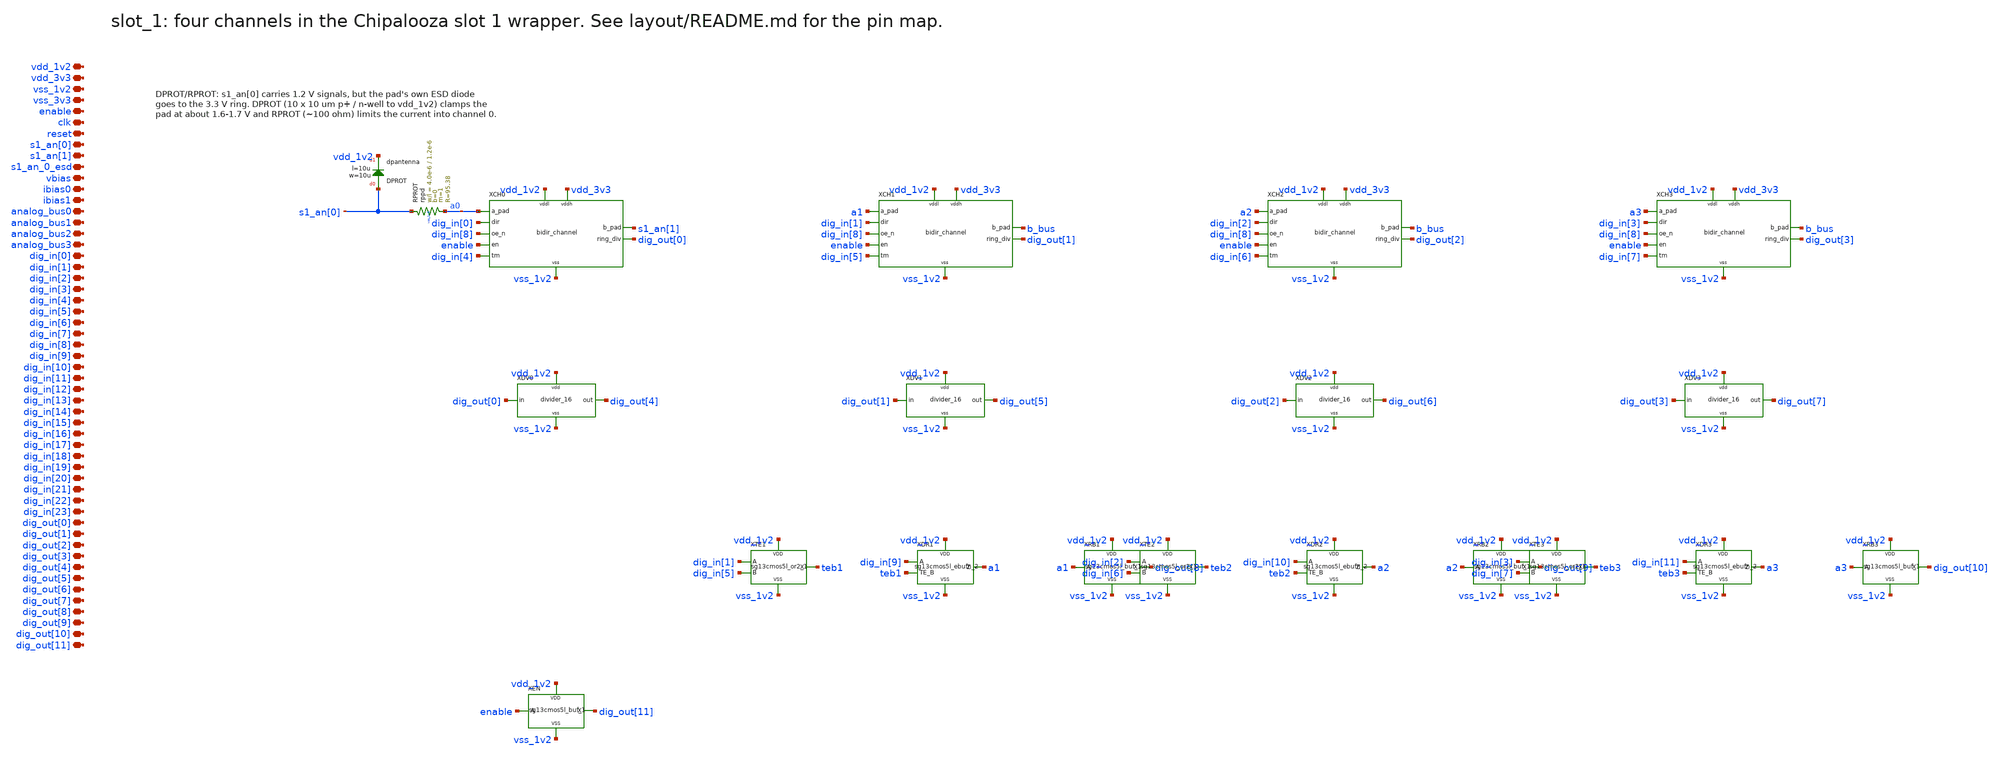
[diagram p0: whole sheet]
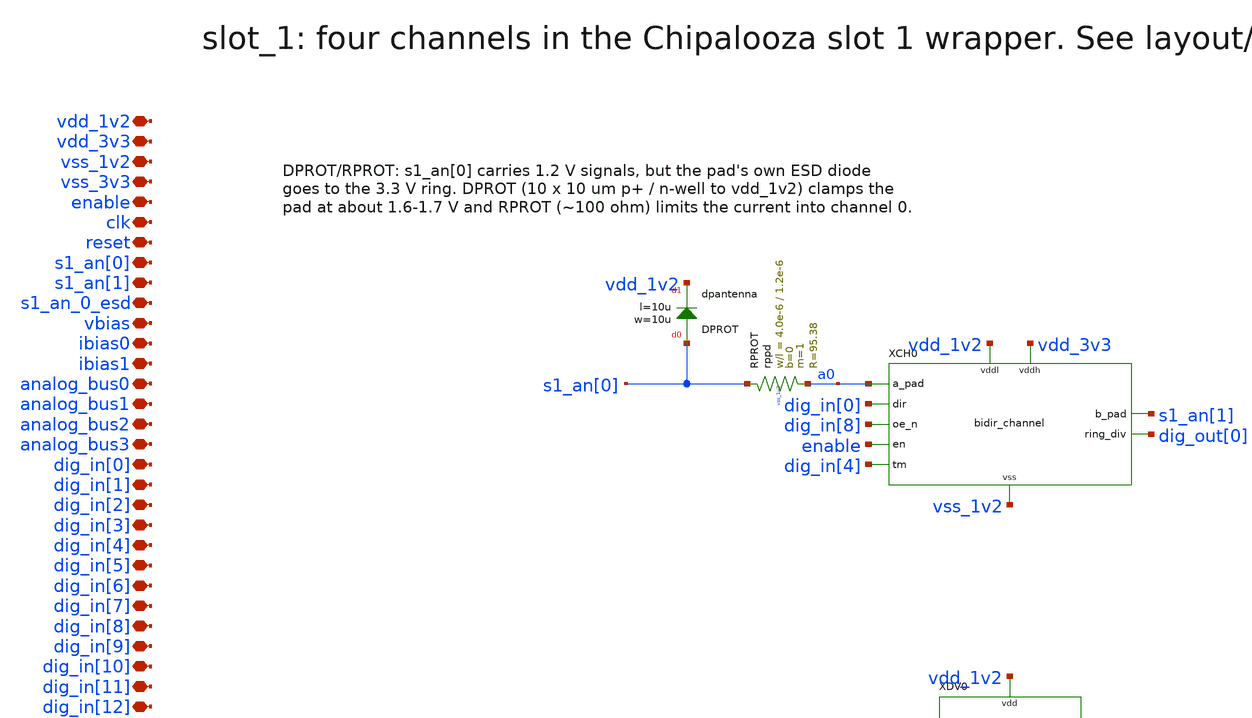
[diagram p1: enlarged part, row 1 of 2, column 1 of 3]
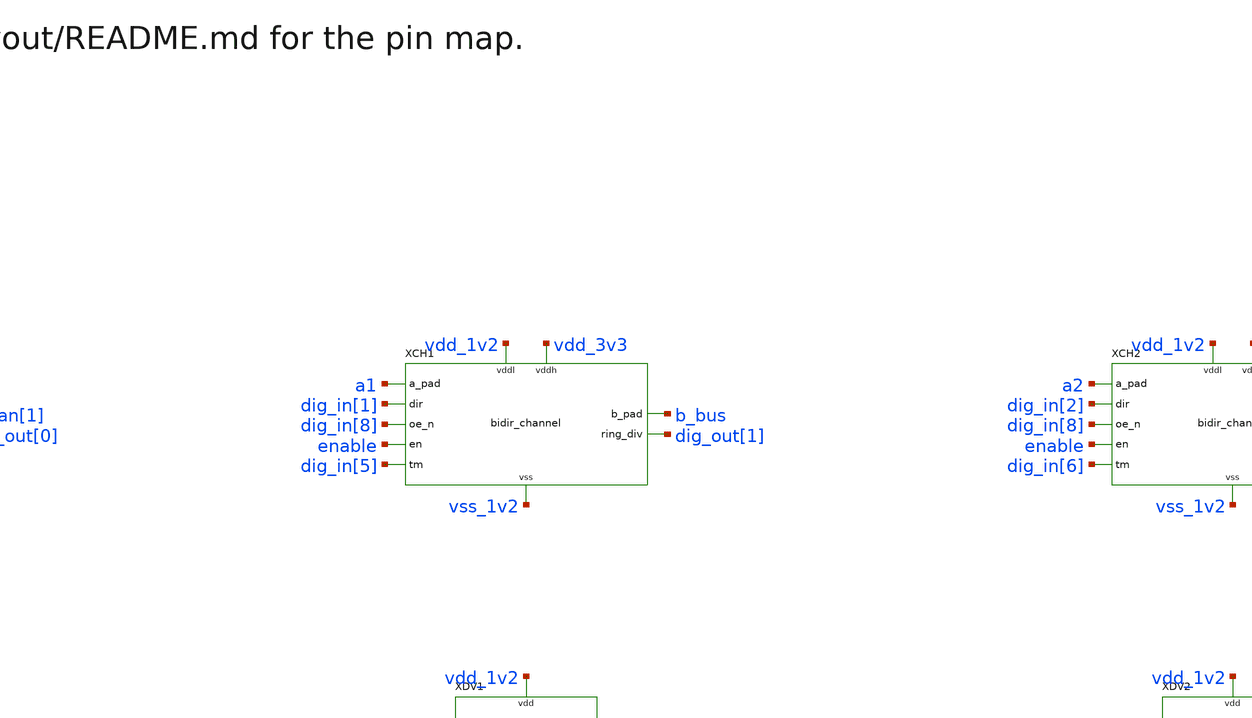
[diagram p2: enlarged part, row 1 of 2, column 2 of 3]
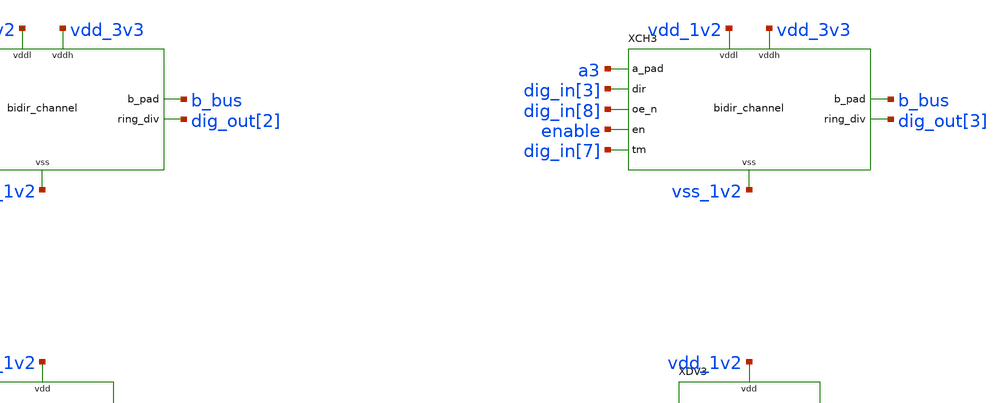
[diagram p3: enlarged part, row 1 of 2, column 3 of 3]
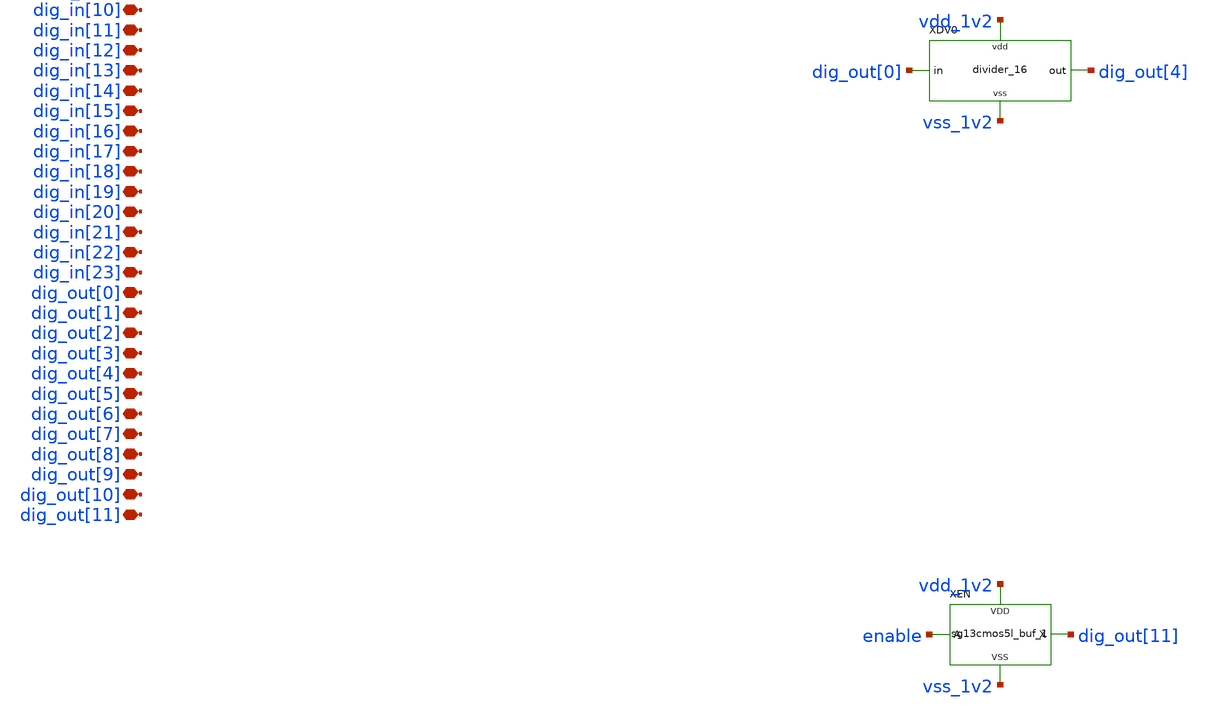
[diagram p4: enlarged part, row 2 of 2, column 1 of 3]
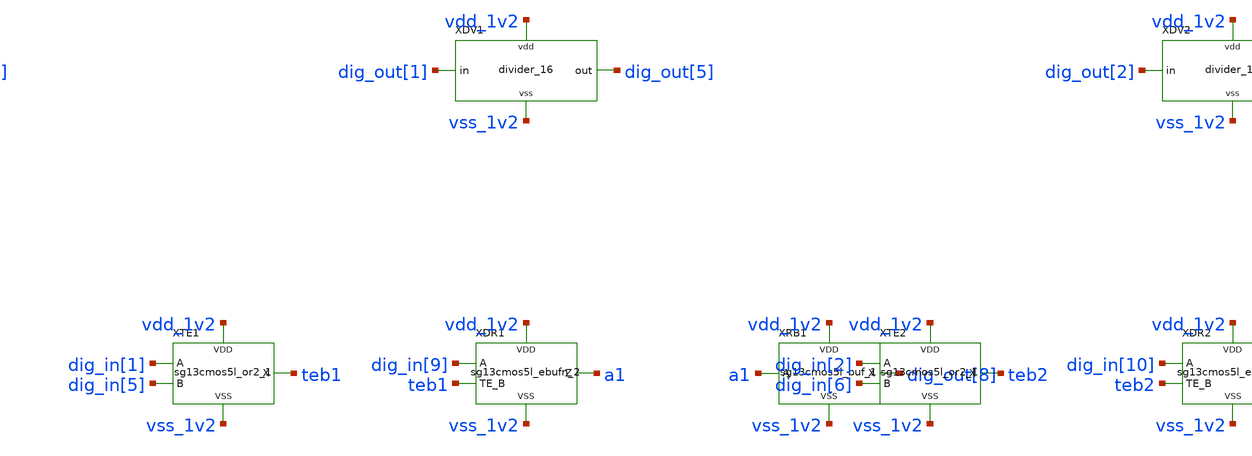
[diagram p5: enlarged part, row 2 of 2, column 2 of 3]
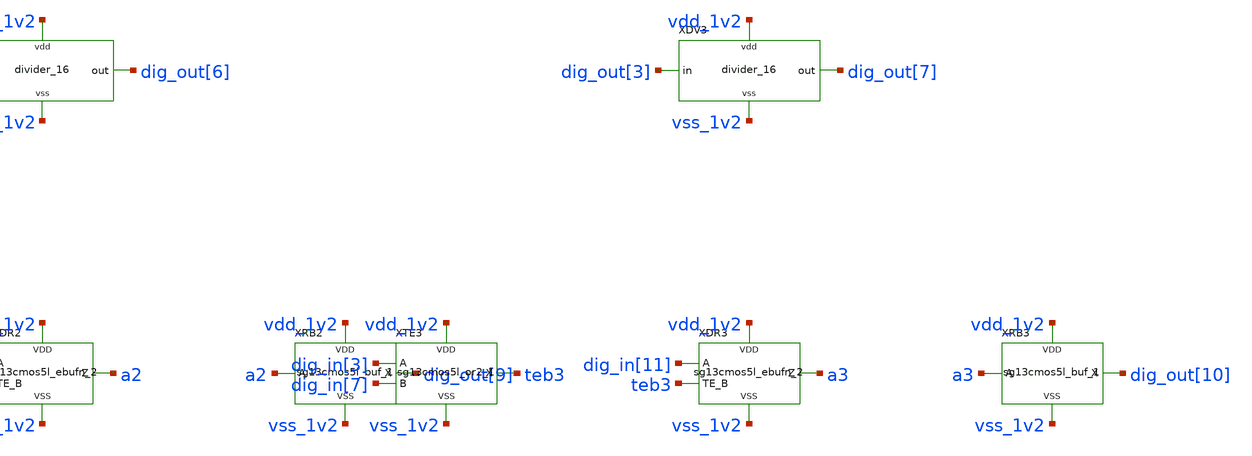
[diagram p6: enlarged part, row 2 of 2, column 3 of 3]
** sch_path: xschem/schematics/slot_1.sch
**.subckt slot_1 vdd_1v2 vdd_3v3 vss_1v2 vss_3v3 enable clk reset s1_an[0] s1_an[1] s1_an_0_esd
*+ vbias ibias0 ibias1 analog_bus0 analog_bus1 analog_bus2 analog_bus3 dig_in[0] dig_in[1] dig_in[2]
*+ dig_in[3] dig_in[4] dig_in[5] dig_in[6] dig_in[7] dig_in[8] dig_in[9] dig_in[10] dig_in[11] dig_in[12]
*+ dig_in[13] dig_in[14] dig_in[15] dig_in[16] dig_in[17] dig_in[18] dig_in[19] dig_in[20] dig_in[21] dig_in[22]
*+ dig_in[23] dig_out[0] dig_out[1] dig_out[2] dig_out[3] dig_out[4] dig_out[5] dig_out[6] dig_out[7] dig_out[8]
*+ dig_out[9] dig_out[10] dig_out[11]
*.iopin vdd_1v2
*.iopin vdd_3v3
*.iopin vss_1v2
*.iopin vss_3v3
*.iopin enable
*.iopin clk
*.iopin reset
*.iopin s1_an[0]
*.iopin s1_an[1]
*.iopin s1_an_0_esd
*.iopin vbias
*.iopin ibias0
*.iopin ibias1
*.iopin analog_bus0
*.iopin analog_bus1
*.iopin analog_bus2
*.iopin analog_bus3
*.iopin dig_in[0]
*.iopin dig_in[1]
*.iopin dig_in[2]
*.iopin dig_in[3]
*.iopin dig_in[4]
*.iopin dig_in[5]
*.iopin dig_in[6]
*.iopin dig_in[7]
*.iopin dig_in[8]
*.iopin dig_in[9]
*.iopin dig_in[10]
*.iopin dig_in[11]
*.iopin dig_in[12]
*.iopin dig_in[13]
*.iopin dig_in[14]
*.iopin dig_in[15]
*.iopin dig_in[16]
*.iopin dig_in[17]
*.iopin dig_in[18]
*.iopin dig_in[19]
*.iopin dig_in[20]
*.iopin dig_in[21]
*.iopin dig_in[22]
*.iopin dig_in[23]
*.iopin dig_out[0]
*.iopin dig_out[1]
*.iopin dig_out[2]
*.iopin dig_out[3]
*.iopin dig_out[4]
*.iopin dig_out[5]
*.iopin dig_out[6]
*.iopin dig_out[7]
*.iopin dig_out[8]
*.iopin dig_out[9]
*.iopin dig_out[10]
*.iopin dig_out[11]
XCH0 a0 s1_an[1] dig_in[0] dig_in[8] enable dig_in[4] dig_out[0] vdd_1v2 vdd_3v3 vss_1v2
+ bidir_channel
XRPROT s1_an[0] a0 vss_1v2 rppd w=4.0e-6 l=1.2e-6 m=1 b=0 mm_ok=1
XDPROT s1_an[0] vdd_1v2 dpantenna l=10u w=10u
XDV0 dig_out[0] dig_out[4] vdd_1v2 vss_1v2 divider_16
XCH1 a1 b_bus dig_in[1] dig_in[8] enable dig_in[5] dig_out[1] vdd_1v2 vdd_3v3 vss_1v2 bidir_channel
XDV1 dig_out[1] dig_out[5] vdd_1v2 vss_1v2 divider_16
XTE1 teb1 dig_in[1] dig_in[5] vdd_1v2 vss_1v2 sg13cmos5l_or2_1
XDR1 a1 dig_in[9] teb1 vdd_1v2 vss_1v2 sg13cmos5l_ebufn_2
XRB1 dig_out[8] a1 vdd_1v2 vss_1v2 sg13cmos5l_buf_1
XCH2 a2 b_bus dig_in[2] dig_in[8] enable dig_in[6] dig_out[2] vdd_1v2 vdd_3v3 vss_1v2 bidir_channel
XDV2 dig_out[2] dig_out[6] vdd_1v2 vss_1v2 divider_16
XTE2 teb2 dig_in[2] dig_in[6] vdd_1v2 vss_1v2 sg13cmos5l_or2_1
XDR2 a2 dig_in[10] teb2 vdd_1v2 vss_1v2 sg13cmos5l_ebufn_2
XRB2 dig_out[9] a2 vdd_1v2 vss_1v2 sg13cmos5l_buf_1
XCH3 a3 b_bus dig_in[3] dig_in[8] enable dig_in[7] dig_out[3] vdd_1v2 vdd_3v3 vss_1v2 bidir_channel
XDV3 dig_out[3] dig_out[7] vdd_1v2 vss_1v2 divider_16
XTE3 teb3 dig_in[3] dig_in[7] vdd_1v2 vss_1v2 sg13cmos5l_or2_1
XDR3 a3 dig_in[11] teb3 vdd_1v2 vss_1v2 sg13cmos5l_ebufn_2
XRB3 dig_out[10] a3 vdd_1v2 vss_1v2 sg13cmos5l_buf_1
XEN dig_out[11] enable vdd_1v2 vss_1v2 sg13cmos5l_buf_1
**.ends
.end
